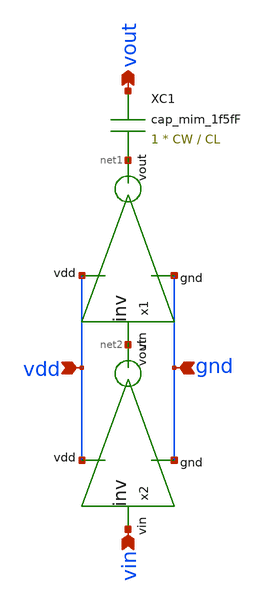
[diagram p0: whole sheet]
** sch_path: symbols/cdac_line.sch
**.subckt cdac_line vdd gnd vin vout
*.ipin vdd
*.ipin gnd
*.ipin vin
*.opin vout
x1 vdd gnd net1 net2 inv cl=0.28u wp=0.66u wn=0.22u
XC1 vout net1 cap_mim_1f5fF c_width=CW c_length=CL m=1
x2 vdd gnd net2 vin inv cl=0.28u wp=0.66u wn=0.22u
**.ends

* expanding   symbol:  /foss/designs/sar_adc/xschem/spice/inv.sym # of pins=4
** sym_path: /foss/designs/sar_adc/xschem/spice/inv.sym
** sch_path: /foss/designs/sar_adc/xschem/spice/inv.sch
.subckt inv vdd gnd vout vin  cl=0.28u wp=0.44u wn=0.22u
*.ipin gnd
*.ipin vdd
*.ipin vin
*.opin vout
XM1 gnd vin vout gnd nfet_03v3 L=0.28u W=.22u nf=1 ad='int((nf+1)/2) * W/nf * 0.18u' as='int((nf+2)/2) * W/nf * 0.18u'
+ pd='2*int((nf+1)/2) * (W/nf + 0.18u)' ps='2*int((nf+2)/2) * (W/nf + 0.18u)' nrd='0.18u / W' nrs='0.18u / W'
+ sa=0 sb=0 sd=0 m=1
XM2 vdd vin vout vdd pfet_03v3 L=0.28u W=.22u nf=1 ad='int((nf+1)/2) * W/nf * 0.18u' as='int((nf+2)/2) * W/nf * 0.18u'
+ pd='2*int((nf+1)/2) * (W/nf + 0.18u)' ps='2*int((nf+2)/2) * (W/nf + 0.18u)' nrd='0.18u / W' nrs='0.18u / W'
+ sa=0 sb=0 sd=0 m=1
.ends

.end
